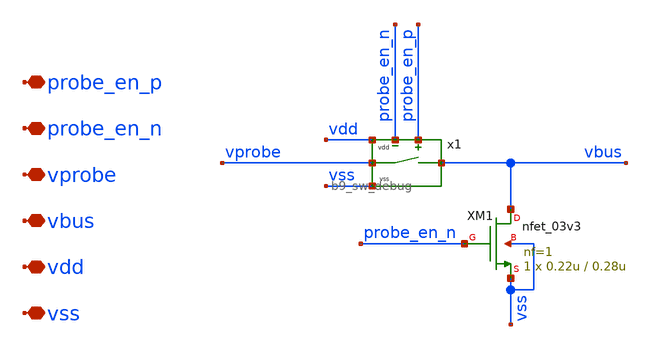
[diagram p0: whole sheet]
** sch_path: xschem/debug_mux/b9_debug_bitcell_local.sch
**.subckt b9_debug_bitcell_local probe_en_p probe_en_n vprobe vbus vdd vss
*.iopin probe_en_p
*.iopin probe_en_n
*.iopin vprobe
*.iopin vbus
*.iopin vdd
*.iopin vss
x1 vdd vprobe vss vbus probe_en_n probe_en_p b9_sw_debug
XM1 vbus probe_en_n vss vss nfet_03v3 L=0.28u W=0.22u nf=1 ad='int((nf+1)/2) * W/nf * 0.18u' as='int((nf+2)/2) * W/nf * 0.18u'
+ pd='2*int((nf+1)/2) * (W/nf + 0.18u)' ps='2*int((nf+2)/2) * (W/nf + 0.18u)' nrd='0.18u / W' nrs='0.18u / W'
+ sa=0 sb=0 sd=0 m=1
**.ends

* expanding   symbol:  xschem/sw/b9_sw_debug.sym # of pins=6
** sym_path: xschem/sw/b9_sw_debug.sym
** sch_path: xschem/sw/b9_sw_debug.sch
.subckt b9_sw_debug vdd va vss vb en_n en
*.iopin vdd
*.iopin vss
*.iopin en
*.iopin va
*.iopin vb
*.iopin en_n
XM1 vb en va vss nfet_03v3 L=0.28u W=3.2u nf=4 ad='int((nf+1)/2) * W/nf * 0.18u' as='int((nf+2)/2) * W/nf * 0.18u'
+ pd='2*int((nf+1)/2) * (W/nf + 0.18u)' ps='2*int((nf+2)/2) * (W/nf + 0.18u)' nrd='0.18u / W' nrs='0.18u / W'
+ sa=0 sb=0 sd=0 m=1
XM2 va en_n vb vdd pfet_03v3 L=0.28u W=9.6u nf=4 ad='int((nf+1)/2) * W/nf * 0.18u' as='int((nf+2)/2) * W/nf * 0.18u'
+ pd='2*int((nf+1)/2) * (W/nf + 0.18u)' ps='2*int((nf+2)/2) * (W/nf + 0.18u)' nrd='0.18u / W' nrs='0.18u / W'
+ sa=0 sb=0 sd=0 m=1
.ends

.end
